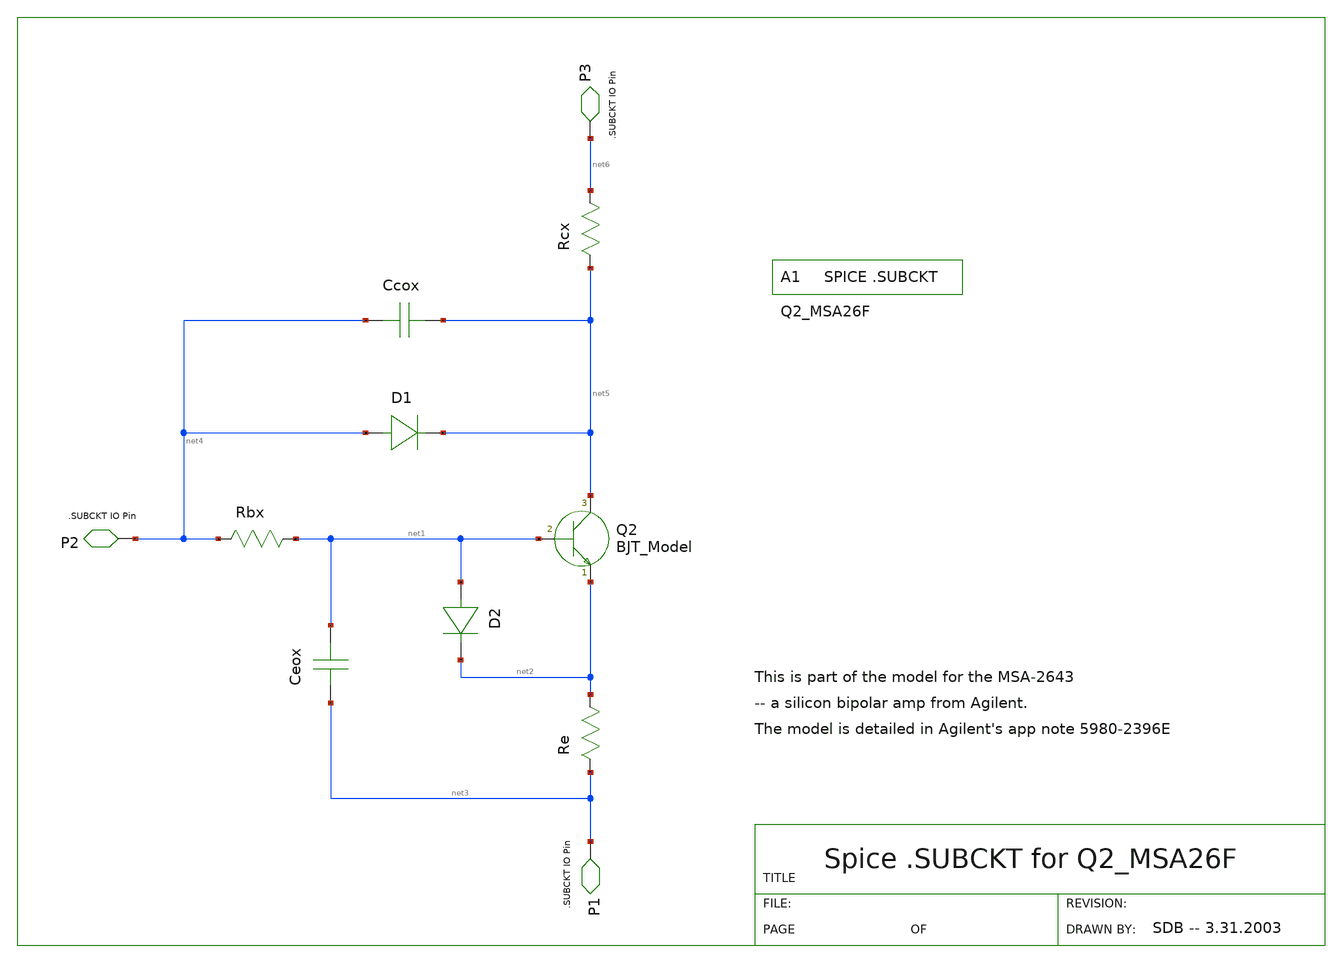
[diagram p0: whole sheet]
** sch_path: xschem-src/xschem_library/gschem_import/Q2.sch
* Copyright (C) 1998-2026 Stefan Frederik Schippers
* This program is free software; you can redistribute it and/or modify
* it under the terms of the GNU General Public License as published by
* the Free Software Foundation; either version 2 of the License, or
* (at your option) any later version.
* This program is distributed in the hope that it will be useful,
* but WITHOUT ANY WARRANTY; without even the implied warranty of
* MERCHANTABILITY or FITNESS FOR A PARTICULAR PURPOSE.  See the
* GNU General Public License for more details.
* You should have received a copy of the GNU General Public License
* along with this program; if not, write to the Free Software
**.subckt Q2
Q2 net5 net1 net2
D1 net4 net5
D2 net1 net2
Ccox net4 net5 6.598e-14F
Ceox net3 net1 2.417e-14F
Rbx net4 net1 0.463
Rcx net5 net6 1.716
Re net3 net2 0.443
P3 net6
P2 net4
P1 net3
A1
**.ends
.end
